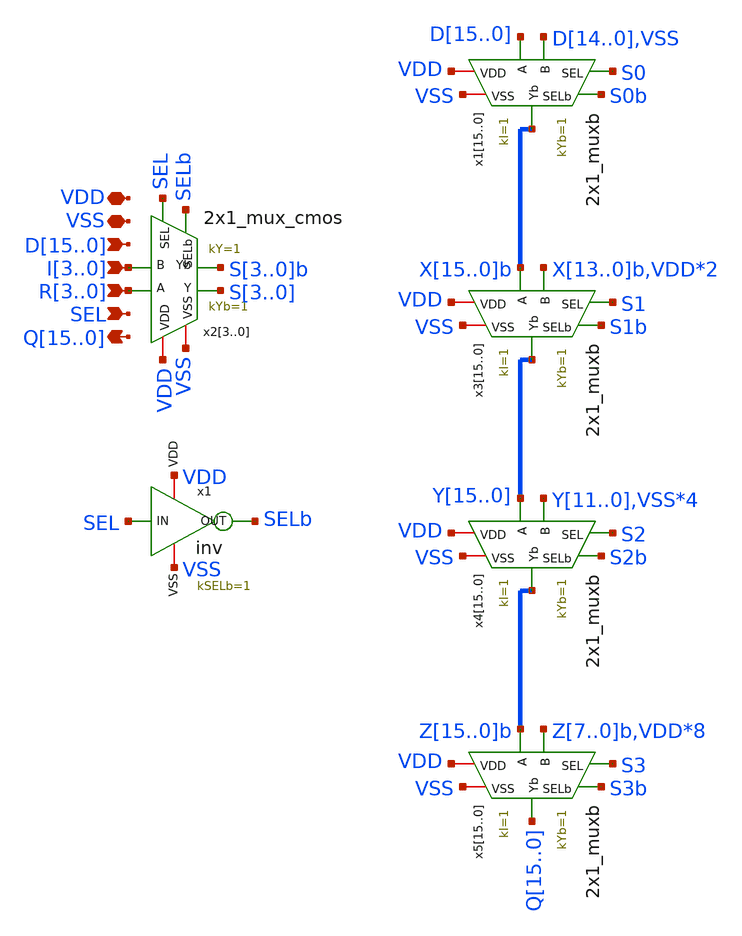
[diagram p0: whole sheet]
** sch_path: CAD5/shifter.sch
**.subckt shifter VDD VSS D15,D14,D13,D12,D11,D10,D9,D8,D7,D6,D5,D4,D3,D2,D1,D0
*+ Q15,Q14,Q13,Q12,Q11,Q10,Q9,Q8,Q7,Q6,Q5,Q4,Q3,Q2,Q1,Q0 R3,R2,R1,R0 I3,I2,I1,I0 SEL
*.iopin VDD
*.iopin VSS
*.ipin D15,D14,D13,D12,D11,D10,D9,D8,D7,D6,D5,D4,D3,D2,D1,D0
*.opin Q15,Q14,Q13,Q12,Q11,Q10,Q9,Q8,Q7,Q6,Q5,Q4,Q3,Q2,Q1,Q0
*.ipin R3,R2,R1,R0
*.ipin I3,I2,I1,I0
*.ipin SEL
x115 D15 S0 S0b VDD VSS D14 X15b 2x1_muxb kI=1 kYb=1
x114 D14 S0 S0b VDD VSS D13 X14b 2x1_muxb kI=1 kYb=1
x113 D13 S0 S0b VDD VSS D12 X13b 2x1_muxb kI=1 kYb=1
x112 D12 S0 S0b VDD VSS D11 X12b 2x1_muxb kI=1 kYb=1
x111 D11 S0 S0b VDD VSS D10 X11b 2x1_muxb kI=1 kYb=1
x110 D10 S0 S0b VDD VSS D9 X10b 2x1_muxb kI=1 kYb=1
x19 D9 S0 S0b VDD VSS D8 X9b 2x1_muxb kI=1 kYb=1
x18 D8 S0 S0b VDD VSS D7 X8b 2x1_muxb kI=1 kYb=1
x17 D7 S0 S0b VDD VSS D6 X7b 2x1_muxb kI=1 kYb=1
x16 D6 S0 S0b VDD VSS D5 X6b 2x1_muxb kI=1 kYb=1
x15 D5 S0 S0b VDD VSS D4 X5b 2x1_muxb kI=1 kYb=1
x14 D4 S0 S0b VDD VSS D3 X4b 2x1_muxb kI=1 kYb=1
x13 D3 S0 S0b VDD VSS D2 X3b 2x1_muxb kI=1 kYb=1
x12 D2 S0 S0b VDD VSS D1 X2b 2x1_muxb kI=1 kYb=1
x11 D1 S0 S0b VDD VSS D0 X1b 2x1_muxb kI=1 kYb=1
x10 D0 S0 S0b VDD VSS VSS X0b 2x1_muxb kI=1 kYb=1
x23 R3 SEL SELb S3 VDD VSS I3 S3b 2x1_mux_cmos kYb=1 kY=1
x22 R2 SEL SELb S2 VDD VSS I2 S2b 2x1_mux_cmos kYb=1 kY=1
x21 R1 SEL SELb S1 VDD VSS I1 S1b 2x1_mux_cmos kYb=1 kY=1
x20 R0 SEL SELb S0 VDD VSS I0 S0b 2x1_mux_cmos kYb=1 kY=1
x1 VDD SEL SELb VSS inv kSELb=1
x315 X15b S1 S1b VDD VSS X13b Y15 2x1_muxb kI=1 kYb=1
x314 X14b S1 S1b VDD VSS X12b Y14 2x1_muxb kI=1 kYb=1
x313 X13b S1 S1b VDD VSS X11b Y13 2x1_muxb kI=1 kYb=1
x312 X12b S1 S1b VDD VSS X10b Y12 2x1_muxb kI=1 kYb=1
x311 X11b S1 S1b VDD VSS X9b Y11 2x1_muxb kI=1 kYb=1
x310 X10b S1 S1b VDD VSS X8b Y10 2x1_muxb kI=1 kYb=1
x39 X9b S1 S1b VDD VSS X7b Y9 2x1_muxb kI=1 kYb=1
x38 X8b S1 S1b VDD VSS X6b Y8 2x1_muxb kI=1 kYb=1
x37 X7b S1 S1b VDD VSS X5b Y7 2x1_muxb kI=1 kYb=1
x36 X6b S1 S1b VDD VSS X4b Y6 2x1_muxb kI=1 kYb=1
x35 X5b S1 S1b VDD VSS X3b Y5 2x1_muxb kI=1 kYb=1
x34 X4b S1 S1b VDD VSS X2b Y4 2x1_muxb kI=1 kYb=1
x33 X3b S1 S1b VDD VSS X1b Y3 2x1_muxb kI=1 kYb=1
x32 X2b S1 S1b VDD VSS X0b Y2 2x1_muxb kI=1 kYb=1
x31 X1b S1 S1b VDD VSS VDD Y1 2x1_muxb kI=1 kYb=1
x30 X0b S1 S1b VDD VSS VDD Y0 2x1_muxb kI=1 kYb=1
x415 Y15 S2 S2b VDD VSS Y11 Z15b 2x1_muxb kI=1 kYb=1
x414 Y14 S2 S2b VDD VSS Y10 Z14b 2x1_muxb kI=1 kYb=1
x413 Y13 S2 S2b VDD VSS Y9 Z13b 2x1_muxb kI=1 kYb=1
x412 Y12 S2 S2b VDD VSS Y8 Z12b 2x1_muxb kI=1 kYb=1
x411 Y11 S2 S2b VDD VSS Y7 Z11b 2x1_muxb kI=1 kYb=1
x410 Y10 S2 S2b VDD VSS Y6 Z10b 2x1_muxb kI=1 kYb=1
x49 Y9 S2 S2b VDD VSS Y5 Z9b 2x1_muxb kI=1 kYb=1
x48 Y8 S2 S2b VDD VSS Y4 Z8b 2x1_muxb kI=1 kYb=1
x47 Y7 S2 S2b VDD VSS Y3 Z7b 2x1_muxb kI=1 kYb=1
x46 Y6 S2 S2b VDD VSS Y2 Z6b 2x1_muxb kI=1 kYb=1
x45 Y5 S2 S2b VDD VSS Y1 Z5b 2x1_muxb kI=1 kYb=1
x44 Y4 S2 S2b VDD VSS Y0 Z4b 2x1_muxb kI=1 kYb=1
x43 Y3 S2 S2b VDD VSS VSS Z3b 2x1_muxb kI=1 kYb=1
x42 Y2 S2 S2b VDD VSS VSS Z2b 2x1_muxb kI=1 kYb=1
x41 Y1 S2 S2b VDD VSS VSS Z1b 2x1_muxb kI=1 kYb=1
x40 Y0 S2 S2b VDD VSS VSS Z0b 2x1_muxb kI=1 kYb=1
x515 Z15b S3 S3b VDD VSS Z7b Q15 2x1_muxb kI=1 kYb=1
x514 Z14b S3 S3b VDD VSS Z6b Q14 2x1_muxb kI=1 kYb=1
x513 Z13b S3 S3b VDD VSS Z5b Q13 2x1_muxb kI=1 kYb=1
x512 Z12b S3 S3b VDD VSS Z4b Q12 2x1_muxb kI=1 kYb=1
x511 Z11b S3 S3b VDD VSS Z3b Q11 2x1_muxb kI=1 kYb=1
x510 Z10b S3 S3b VDD VSS Z2b Q10 2x1_muxb kI=1 kYb=1
x59 Z9b S3 S3b VDD VSS Z1b Q9 2x1_muxb kI=1 kYb=1
x58 Z8b S3 S3b VDD VSS Z0b Q8 2x1_muxb kI=1 kYb=1
x57 Z7b S3 S3b VDD VSS VDD Q7 2x1_muxb kI=1 kYb=1
x56 Z6b S3 S3b VDD VSS VDD Q6 2x1_muxb kI=1 kYb=1
x55 Z5b S3 S3b VDD VSS VDD Q5 2x1_muxb kI=1 kYb=1
x54 Z4b S3 S3b VDD VSS VDD Q4 2x1_muxb kI=1 kYb=1
x53 Z3b S3 S3b VDD VSS VDD Q3 2x1_muxb kI=1 kYb=1
x52 Z2b S3 S3b VDD VSS VDD Q2 2x1_muxb kI=1 kYb=1
x51 Z1b S3 S3b VDD VSS VDD Q1 2x1_muxb kI=1 kYb=1
x50 Z0b S3 S3b VDD VSS VDD Q0 2x1_muxb kI=1 kYb=1
**.ends

* expanding   symbol:  engn1600-team1/CAD5/2x1_muxb.sym # of pins=7
** sym_path: CAD5/2x1_muxb.sym
** sch_path: CAD5/2x1_muxb.sch
.subckt 2x1_muxb A SEL SELb VDD VSS B Yb  kI=1 kYb=1
*.ipin A
*.ipin B
*.ipin SEL
*.iopin VDD
*.iopin VSS
*.ipin SELb
*.opin Yb
XM1 VSS B net1 VSS nfet_03v3 L=0.28u W='kI*0.36u' nf=1 ad='int((nf+1)/2) * W/nf * 0.18u' as='int((nf+2)/2) * W/nf * 0.18u'
+ pd='2*int((nf+1)/2) * (W/nf + 0.18u)' ps='2*int((nf+2)/2) * (W/nf + 0.18u)' nrd='0.18u / W' nrs='0.18u / W'
+ sa=0 sb=0 sd=0 m=1
XM2 net1 SEL Yb VSS nfet_03v3 L=0.28u W='kYb*0.36u' nf=1 ad='int((nf+1)/2) * W/nf * 0.18u' as='int((nf+2)/2) * W/nf * 0.18u'
+ pd='2*int((nf+1)/2) * (W/nf + 0.18u)' ps='2*int((nf+2)/2) * (W/nf + 0.18u)' nrd='0.18u / W' nrs='0.18u / W'
+ sa=0 sb=0 sd=0 m=1
XM3 Yb SELb net2 VSS nfet_03v3 L=0.28u W='kYb*0.36u' nf=1 ad='int((nf+1)/2) * W/nf * 0.18u' as='int((nf+2)/2) * W/nf * 0.18u'
+ pd='2*int((nf+1)/2) * (W/nf + 0.18u)' ps='2*int((nf+2)/2) * (W/nf + 0.18u)' nrd='0.18u / W' nrs='0.18u / W'
+ sa=0 sb=0 sd=0 m=1
XM4 net2 A VSS VSS nfet_03v3 L=0.28u W='kI*0.36u' nf=1 ad='int((nf+1)/2) * W/nf * 0.18u' as='int((nf+2)/2) * W/nf * 0.18u'
+ pd='2*int((nf+1)/2) * (W/nf + 0.18u)' ps='2*int((nf+2)/2) * (W/nf + 0.18u)' nrd='0.18u / W' nrs='0.18u / W'
+ sa=0 sb=0 sd=0 m=1
XM5 net3 SELb Yb VDD pfet_03v3 L=0.28u W='kYb*0.72u' nf=1 ad='int((nf+1)/2) * W/nf * 0.18u' as='int((nf+2)/2) * W/nf * 0.18u'
+ pd='2*int((nf+1)/2) * (W/nf + 0.18u)' ps='2*int((nf+2)/2) * (W/nf + 0.18u)' nrd='0.18u / W' nrs='0.18u / W'
+ sa=0 sb=0 sd=0 m=1
XM6 VDD B net3 VDD pfet_03v3 L=0.28u W='kI*0.72u' nf=1 ad='int((nf+1)/2) * W/nf * 0.18u' as='int((nf+2)/2) * W/nf * 0.18u'
+ pd='2*int((nf+1)/2) * (W/nf + 0.18u)' ps='2*int((nf+2)/2) * (W/nf + 0.18u)' nrd='0.18u / W' nrs='0.18u / W'
+ sa=0 sb=0 sd=0 m=1
XM7 net4 A VDD VDD pfet_03v3 L=0.28u W='kI*0.72u' nf=1 ad='int((nf+1)/2) * W/nf * 0.18u' as='int((nf+2)/2) * W/nf * 0.18u'
+ pd='2*int((nf+1)/2) * (W/nf + 0.18u)' ps='2*int((nf+2)/2) * (W/nf + 0.18u)' nrd='0.18u / W' nrs='0.18u / W'
+ sa=0 sb=0 sd=0 m=1
XM8 Yb SEL net4 VDD pfet_03v3 L=0.28u W='kYb*0.72u' nf=1 ad='int((nf+1)/2) * W/nf * 0.18u' as='int((nf+2)/2) * W/nf * 0.18u'
+ pd='2*int((nf+1)/2) * (W/nf + 0.18u)' ps='2*int((nf+2)/2) * (W/nf + 0.18u)' nrd='0.18u / W' nrs='0.18u / W'
+ sa=0 sb=0 sd=0 m=1
**** begin user architecture code


.param kI=1
.param kYb=1


**** end user architecture code
.ends


* expanding   symbol:  engn1600-team1/CAD5/2x1_mux_cmos.sym # of pins=8
** sym_path: CAD4/2x1_mux_cmos.sym
** sch_path: CAD4/2x1_mux_cmos.sch
.subckt 2x1_mux_cmos A SEL SELb Y VDD VSS B Yb  kYb=1 kY=1
*.ipin A
*.ipin B
*.ipin SEL
*.opin Y
*.iopin VDD
*.iopin VSS
*.ipin SELb
*.opin Yb
XM1 VSS B net1 VSS nfet_03v3 L=0.28u W='kI*0.36u' nf=1 ad='int((nf+1)/2) * W/nf * 0.18u' as='int((nf+2)/2) * W/nf * 0.18u'
+ pd='2*int((nf+1)/2) * (W/nf + 0.18u)' ps='2*int((nf+2)/2) * (W/nf + 0.18u)' nrd='0.18u / W' nrs='0.18u / W'
+ sa=0 sb=0 sd=0 m=1
XM2 net1 SEL Yb VSS nfet_03v3 L=0.28u W='kYb*0.36u' nf=1 ad='int((nf+1)/2) * W/nf * 0.18u' as='int((nf+2)/2) * W/nf * 0.18u'
+ pd='2*int((nf+1)/2) * (W/nf + 0.18u)' ps='2*int((nf+2)/2) * (W/nf + 0.18u)' nrd='0.18u / W' nrs='0.18u / W'
+ sa=0 sb=0 sd=0 m=1
XM3 Yb SELb net2 VSS nfet_03v3 L=0.28u W='kYb*0.36u' nf=1 ad='int((nf+1)/2) * W/nf * 0.18u' as='int((nf+2)/2) * W/nf * 0.18u'
+ pd='2*int((nf+1)/2) * (W/nf + 0.18u)' ps='2*int((nf+2)/2) * (W/nf + 0.18u)' nrd='0.18u / W' nrs='0.18u / W'
+ sa=0 sb=0 sd=0 m=1
XM4 net2 A VSS VSS nfet_03v3 L=0.28u W='kI*0.36u' nf=1 ad='int((nf+1)/2) * W/nf * 0.18u' as='int((nf+2)/2) * W/nf * 0.18u'
+ pd='2*int((nf+1)/2) * (W/nf + 0.18u)' ps='2*int((nf+2)/2) * (W/nf + 0.18u)' nrd='0.18u / W' nrs='0.18u / W'
+ sa=0 sb=0 sd=0 m=1
XM5 net3 SELb Yb VDD pfet_03v3 L=0.28u W='kYb*0.72u' nf=1 ad='int((nf+1)/2) * W/nf * 0.18u' as='int((nf+2)/2) * W/nf * 0.18u'
+ pd='2*int((nf+1)/2) * (W/nf + 0.18u)' ps='2*int((nf+2)/2) * (W/nf + 0.18u)' nrd='0.18u / W' nrs='0.18u / W'
+ sa=0 sb=0 sd=0 m=1
XM6 VDD B net3 VDD pfet_03v3 L=0.28u W='kI*0.72u' nf=1 ad='int((nf+1)/2) * W/nf * 0.18u' as='int((nf+2)/2) * W/nf * 0.18u'
+ pd='2*int((nf+1)/2) * (W/nf + 0.18u)' ps='2*int((nf+2)/2) * (W/nf + 0.18u)' nrd='0.18u / W' nrs='0.18u / W'
+ sa=0 sb=0 sd=0 m=1
XM7 net4 A VDD VDD pfet_03v3 L=0.28u W='kI*0.72u' nf=1 ad='int((nf+1)/2) * W/nf * 0.18u' as='int((nf+2)/2) * W/nf * 0.18u'
+ pd='2*int((nf+1)/2) * (W/nf + 0.18u)' ps='2*int((nf+2)/2) * (W/nf + 0.18u)' nrd='0.18u / W' nrs='0.18u / W'
+ sa=0 sb=0 sd=0 m=1
XM8 Yb SEL net4 VDD pfet_03v3 L=0.28u W='kYb*0.72u' nf=1 ad='int((nf+1)/2) * W/nf * 0.18u' as='int((nf+2)/2) * W/nf * 0.18u'
+ pd='2*int((nf+1)/2) * (W/nf + 0.18u)' ps='2*int((nf+2)/2) * (W/nf + 0.18u)' nrd='0.18u / W' nrs='0.18u / W'
+ sa=0 sb=0 sd=0 m=1
XM9 VSS Yb Y VSS nfet_03v3 L=0.28u W='kY*0.36u' nf=1 ad='int((nf+1)/2) * W/nf * 0.18u' as='int((nf+2)/2) * W/nf * 0.18u'
+ pd='2*int((nf+1)/2) * (W/nf + 0.18u)' ps='2*int((nf+2)/2) * (W/nf + 0.18u)' nrd='0.18u / W' nrs='0.18u / W'
+ sa=0 sb=0 sd=0 m=1
XM10 VDD Yb Y VDD pfet_03v3 L=0.28u W='kY*0.72u' nf=1 ad='int((nf+1)/2) * W/nf * 0.18u' as='int((nf+2)/2) * W/nf * 0.18u'
+ pd='2*int((nf+1)/2) * (W/nf + 0.18u)' ps='2*int((nf+2)/2) * (W/nf + 0.18u)' nrd='0.18u / W' nrs='0.18u / W'
+ sa=0 sb=0 sd=0 m=1
**** begin user architecture code


.param kI=2.5
.param kYb=1.875
.param kY=2.1527777777777778


**** end user architecture code
.ends


* expanding   symbol:  engn1600-team1/CAD5/inv.sym # of pins=4
** sym_path: CAD5/inv.sym
** sch_path: CAD5/inv.sch
.subckt inv VDD IN OUT VSS  kSELb=1
*.ipin IN
*.opin OUT
*.iopin VDD
*.iopin VSS
XM1 OUT IN VDD VDD pfet_03v3 L=0.28u W='kSELb*0.72u' nf=1 ad='int((nf+1)/2) * W/nf * 0.18u' as='int((nf+2)/2) * W/nf * 0.18u'
+ pd='2*int((nf+1)/2) * (W/nf + 0.18u)' ps='2*int((nf+2)/2) * (W/nf + 0.18u)' nrd='0.18u / W' nrs='0.18u / W'
+ sa=0 sb=0 sd=0 m=1
XM2 OUT IN VSS VSS nfet_03v3 L=0.28u W='kSELb*0.36u' nf=1 ad='int((nf+1)/2) * W/nf * 0.18u' as='int((nf+2)/2) * W/nf * 0.18u'
+ pd='2*int((nf+1)/2) * (W/nf + 0.18u)' ps='2*int((nf+2)/2) * (W/nf + 0.18u)' nrd='0.18u / W' nrs='0.18u / W'
+ sa=0 sb=0 sd=0 m=1
**** begin user architecture code


.param kSELb=1


**** end user architecture code
.ends

.end
